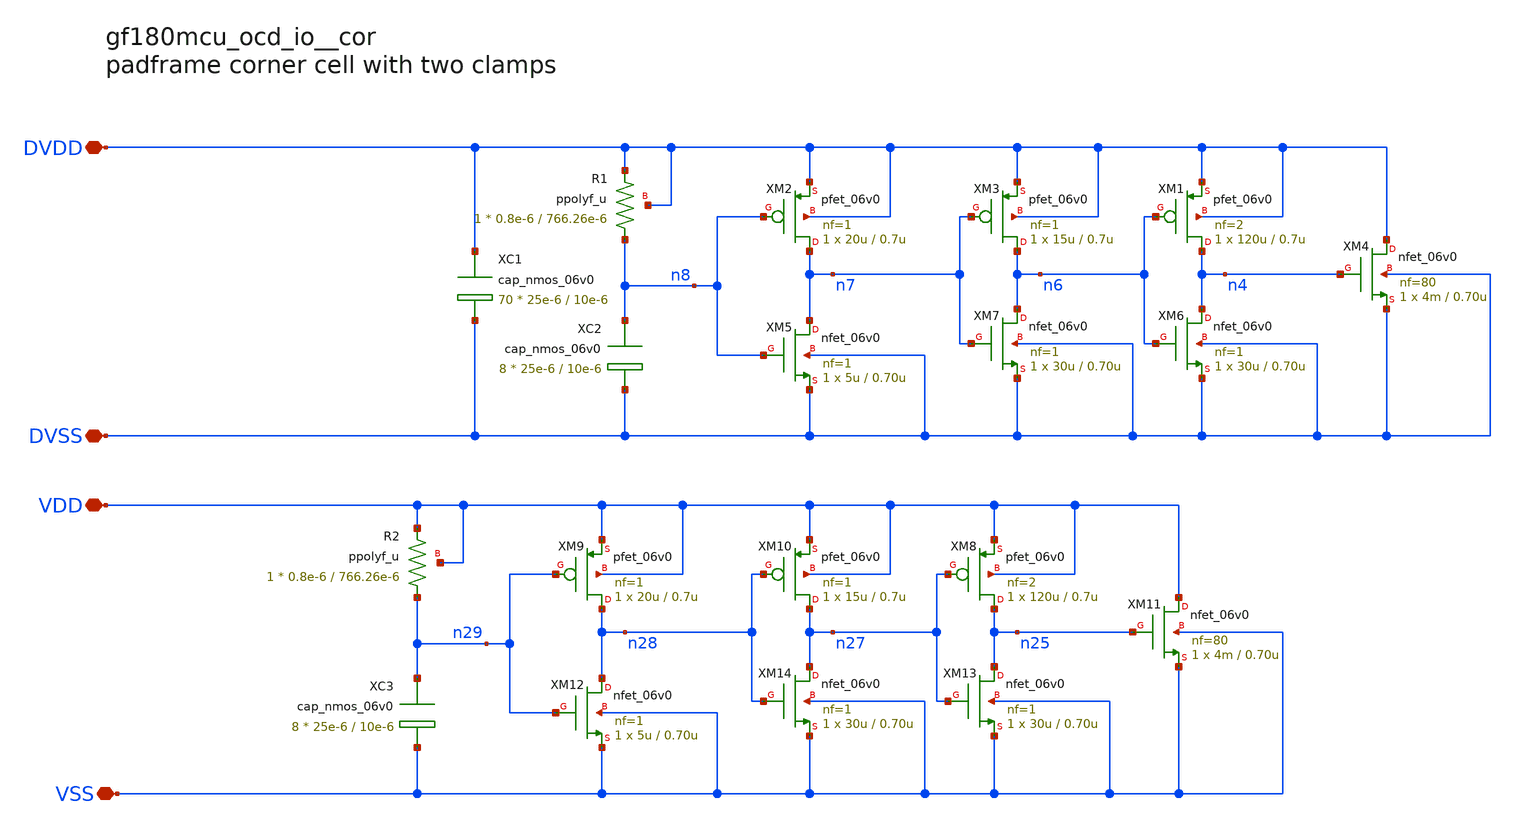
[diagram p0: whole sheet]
** sch_path: cells/cor/gf180mcu_ocd_io__cor.sch
**.subckt gf180mcu_ocd_io__cor DVDD DVSS VSS VDD
*.iopin DVDD
*.iopin DVSS
*.iopin VSS
*.iopin VDD
XC1 DVDD DVSS cap_nmos_06v0 c_width=25e-6 c_length=10e-6 m=70
XM1 n4 n6 DVDD DVDD pfet_06v0 L=0.7u W=120u nf=2 ad='int((nf+1)/2) * W/nf * 0.18u' as='int((nf+2)/2) * W/nf * 0.18u'
+ pd='2*int((nf+1)/2) * (W/nf + 0.18u)' ps='2*int((nf+2)/2) * (W/nf + 0.18u)' nrd='0.18u / W' nrs='0.18u / W'
+ sa=0 sb=0 sd=0 m=1
XM2 n7 n8 DVDD DVDD pfet_06v0 L=0.7u W=20u nf=1 ad='int((nf+1)/2) * W/nf * 0.18u' as='int((nf+2)/2) * W/nf * 0.18u'
+ pd='2*int((nf+1)/2) * (W/nf + 0.18u)' ps='2*int((nf+2)/2) * (W/nf + 0.18u)' nrd='0.18u / W' nrs='0.18u / W'
+ sa=0 sb=0 sd=0 m=1
XM3 n6 n7 DVDD DVDD pfet_06v0 L=0.7u W=15u nf=1 ad='int((nf+1)/2) * W/nf * 0.18u' as='int((nf+2)/2) * W/nf * 0.18u'
+ pd='2*int((nf+1)/2) * (W/nf + 0.18u)' ps='2*int((nf+2)/2) * (W/nf + 0.18u)' nrd='0.18u / W' nrs='0.18u / W'
+ sa=0 sb=0 sd=0 m=1
XC2 n8 DVSS cap_nmos_06v0 c_width=25e-6 c_length=10e-6 m=8
XM4 DVDD n4 DVSS DVSS nfet_06v0 L=0.70u W=4m nf=80 ad='int((nf+1)/2) * W/nf * 0.18u' as='int((nf+2)/2) * W/nf * 0.18u'
+ pd='2*int((nf+1)/2) * (W/nf + 0.18u)' ps='2*int((nf+2)/2) * (W/nf + 0.18u)' nrd='0.18u / W' nrs='0.18u / W'
+ sa=0 sb=0 sd=0 m=1 par=1
XM5 n7 n8 DVSS DVSS nfet_06v0 L=0.70u W=5u nf=1 ad='int((nf+1)/2) * W/nf * 0.18u' as='int((nf+2)/2) * W/nf * 0.18u'
+ pd='2*int((nf+1)/2) * (W/nf + 0.18u)' ps='2*int((nf+2)/2) * (W/nf + 0.18u)' nrd='0.18u / W' nrs='0.18u / W'
+ sa=0 sb=0 sd=0 m=1 par=1
XM6 n4 n6 DVSS DVSS nfet_06v0 L=0.70u W=30u nf=1 ad='int((nf+1)/2) * W/nf * 0.18u' as='int((nf+2)/2) * W/nf * 0.18u'
+ pd='2*int((nf+1)/2) * (W/nf + 0.18u)' ps='2*int((nf+2)/2) * (W/nf + 0.18u)' nrd='0.18u / W' nrs='0.18u / W'
+ sa=0 sb=0 sd=0 m=1 par=1
XM7 n6 n7 DVSS DVSS nfet_06v0 L=0.70u W=30u nf=1 ad='int((nf+1)/2) * W/nf * 0.18u' as='int((nf+2)/2) * W/nf * 0.18u'
+ pd='2*int((nf+1)/2) * (W/nf + 0.18u)' ps='2*int((nf+2)/2) * (W/nf + 0.18u)' nrd='0.18u / W' nrs='0.18u / W'
+ sa=0 sb=0 sd=0 m=1 par=1
XR1 n8 DVDD DVDD ppolyf_u r_width=0.8e-6 r_length=766.26e-6 m=1
XM8 n25 n27 VDD VDD pfet_06v0 L=0.7u W=120u nf=2 ad='int((nf+1)/2) * W/nf * 0.18u' as='int((nf+2)/2) * W/nf * 0.18u'
+ pd='2*int((nf+1)/2) * (W/nf + 0.18u)' ps='2*int((nf+2)/2) * (W/nf + 0.18u)' nrd='0.18u / W' nrs='0.18u / W'
+ sa=0 sb=0 sd=0 m=1
XM9 n28 n29 VDD VDD pfet_06v0 L=0.7u W=20u nf=1 ad='int((nf+1)/2) * W/nf * 0.18u' as='int((nf+2)/2) * W/nf * 0.18u'
+ pd='2*int((nf+1)/2) * (W/nf + 0.18u)' ps='2*int((nf+2)/2) * (W/nf + 0.18u)' nrd='0.18u / W' nrs='0.18u / W'
+ sa=0 sb=0 sd=0 m=1
XM10 n27 n28 VDD VDD pfet_06v0 L=0.7u W=15u nf=1 ad='int((nf+1)/2) * W/nf * 0.18u' as='int((nf+2)/2) * W/nf * 0.18u'
+ pd='2*int((nf+1)/2) * (W/nf + 0.18u)' ps='2*int((nf+2)/2) * (W/nf + 0.18u)' nrd='0.18u / W' nrs='0.18u / W'
+ sa=0 sb=0 sd=0 m=1
XC3 n29 VSS cap_nmos_06v0 c_width=25e-6 c_length=10e-6 m=8
XM11 VDD n25 VSS VSS nfet_06v0 L=0.70u W=4m nf=80 ad='int((nf+1)/2) * W/nf * 0.18u' as='int((nf+2)/2) * W/nf * 0.18u'
+ pd='2*int((nf+1)/2) * (W/nf + 0.18u)' ps='2*int((nf+2)/2) * (W/nf + 0.18u)' nrd='0.18u / W' nrs='0.18u / W'
+ sa=0 sb=0 sd=0 m=1 par=1
XM12 n28 n29 VSS VSS nfet_06v0 L=0.70u W=5u nf=1 ad='int((nf+1)/2) * W/nf * 0.18u' as='int((nf+2)/2) * W/nf * 0.18u'
+ pd='2*int((nf+1)/2) * (W/nf + 0.18u)' ps='2*int((nf+2)/2) * (W/nf + 0.18u)' nrd='0.18u / W' nrs='0.18u / W'
+ sa=0 sb=0 sd=0 m=1 par=1
XM13 n25 n27 VSS VSS nfet_06v0 L=0.70u W=30u nf=1 ad='int((nf+1)/2) * W/nf * 0.18u' as='int((nf+2)/2) * W/nf * 0.18u'
+ pd='2*int((nf+1)/2) * (W/nf + 0.18u)' ps='2*int((nf+2)/2) * (W/nf + 0.18u)' nrd='0.18u / W' nrs='0.18u / W'
+ sa=0 sb=0 sd=0 m=1 par=1
XM14 n27 n28 VSS VSS nfet_06v0 L=0.70u W=30u nf=1 ad='int((nf+1)/2) * W/nf * 0.18u' as='int((nf+2)/2) * W/nf * 0.18u'
+ pd='2*int((nf+1)/2) * (W/nf + 0.18u)' ps='2*int((nf+2)/2) * (W/nf + 0.18u)' nrd='0.18u / W' nrs='0.18u / W'
+ sa=0 sb=0 sd=0 m=1 par=1
XR2 n29 VDD VDD ppolyf_u r_width=0.8e-6 r_length=766.26e-6 m=1
**.ends
.end
